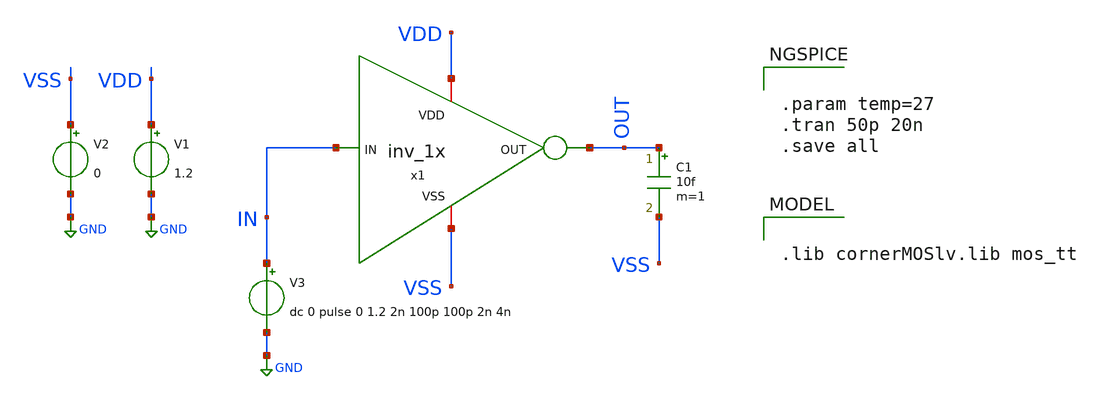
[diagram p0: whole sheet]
** sch_path: designs/1iee34/tb_inv_1x.sch
**.subckt tb_inv_1x
V1 VDD GND 1.2
C1 OUT VSS 10f m=1
V2 VSS GND 0
V3 IN GND dc 0 pulse 0 1.2 2n 100p 100p 2n 4n
x1 VDD IN OUT VSS inv_1x
**** begin user architecture code


.param temp=27
.tran 50p 20n
.save all



.lib cornerMOSlv.lib mos_tt

**** end user architecture code
**.ends

* expanding   symbol:  inv_1x.sym # of pins=4
** sym_path: designs/1iee34/inv_1x.sym
** sch_path: designs/1iee34/inv_1x.sch
.subckt inv_1x VDD IN OUT VSS
*.iopin VDD
*.iopin VSS
*.ipin IN
*.opin OUT
XM1 OUT IN VDD VDD sg13_lv_pmos w=2.0u l=0.13u ng=1 m=1 mm_ok=1
XM2 VSS IN OUT VSS sg13_lv_nmos w=1.0u l=0.13u ng=1 m=1 mm_ok=1
.ends

.GLOBAL GND
.end
